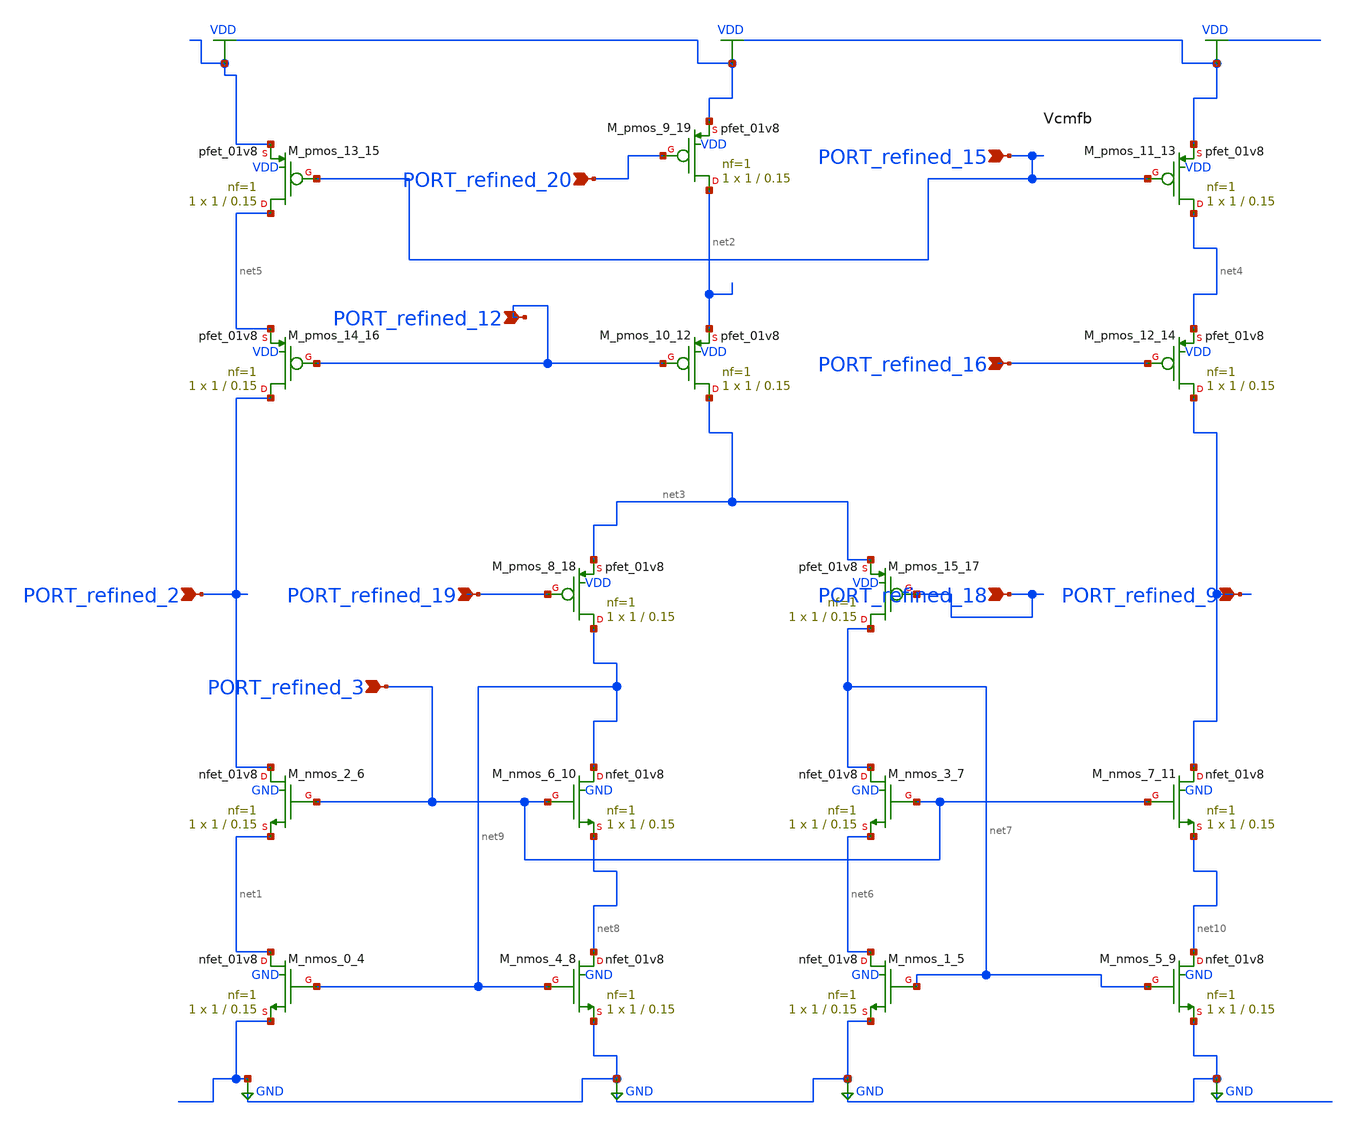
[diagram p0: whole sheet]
** sch_path: schematics/10_1587_elex_17_20200238_02_001_crop2.sch
**.subckt 10_1587_elex_17_20200238_02_001_crop2 PORT_refined_2 PORT_refined_18 PORT_refined_9
*+ PORT_refined_19 PORT_refined_20 PORT_refined_3 PORT_refined_12 PORT_refined_16 PORT_refined_15
*.ipin PORT_refined_2
*.ipin PORT_refined_18
*.ipin PORT_refined_9
*.ipin PORT_refined_19
*.ipin PORT_refined_20
*.ipin PORT_refined_3
*.ipin PORT_refined_12
*.ipin PORT_refined_16
*.ipin PORT_refined_15
XM_nmos_0_4 net1 net9 GND GND sky130_fd_pr__nfet_01v8 L=0.15 W=1 nf=1 ad='int((1 + 1)/2) * 1 / 1 * 0.29'
+ as='int((1 + 2)/2) * 1 / 1 * 0.29' pd='2*int((1 + 1)/2) * (1 / 1 + 0.29)' ps='2*int((1 + 2)/2) * (1 / 1 + 0.29)'
+ nrd='0.29 / 1 ' nrs='0.29 / 1 ' sa=0 sb=0 sd=0 mult=1 m=1
XM_nmos_1_5 net6 net7 GND GND sky130_fd_pr__nfet_01v8 L=0.15 W=1 nf=1 ad='int((1 + 1)/2) * 1 / 1 * 0.29'
+ as='int((1 + 2)/2) * 1 / 1 * 0.29' pd='2*int((1 + 1)/2) * (1 / 1 + 0.29)' ps='2*int((1 + 2)/2) * (1 / 1 + 0.29)'
+ nrd='0.29 / 1 ' nrs='0.29 / 1 ' sa=0 sb=0 sd=0 mult=1 m=1
XM_nmos_2_6 PORT_refined_2 PORT_refined_3 net1 GND sky130_fd_pr__nfet_01v8 L=0.15 W=1 nf=1 ad='int((1 + 1)/2) * 1 / 1 * 0.29'
+ as='int((1 + 2)/2) * 1 / 1 * 0.29' pd='2*int((1 + 1)/2) * (1 / 1 + 0.29)' ps='2*int((1 + 2)/2) * (1 / 1 + 0.29)'
+ nrd='0.29 / 1 ' nrs='0.29 / 1 ' sa=0 sb=0 sd=0 mult=1 m=1
XM_nmos_3_7 net7 PORT_refined_3 net6 GND sky130_fd_pr__nfet_01v8 L=0.15 W=1 nf=1 ad='int((1 + 1)/2) * 1 / 1 * 0.29'
+ as='int((1 + 2)/2) * 1 / 1 * 0.29' pd='2*int((1 + 1)/2) * (1 / 1 + 0.29)' ps='2*int((1 + 2)/2) * (1 / 1 + 0.29)'
+ nrd='0.29 / 1 ' nrs='0.29 / 1 ' sa=0 sb=0 sd=0 mult=1 m=1
XM_nmos_4_8 net8 net9 GND GND sky130_fd_pr__nfet_01v8 L=0.15 W=1 nf=1 ad='int((1 + 1)/2) * 1 / 1 * 0.29'
+ as='int((1 + 2)/2) * 1 / 1 * 0.29' pd='2*int((1 + 1)/2) * (1 / 1 + 0.29)' ps='2*int((1 + 2)/2) * (1 / 1 + 0.29)'
+ nrd='0.29 / 1 ' nrs='0.29 / 1 ' sa=0 sb=0 sd=0 mult=1 m=1
XM_nmos_5_9 net10 net7 GND GND sky130_fd_pr__nfet_01v8 L=0.15 W=1 nf=1 ad='int((1 + 1)/2) * 1 / 1 * 0.29'
+ as='int((1 + 2)/2) * 1 / 1 * 0.29' pd='2*int((1 + 1)/2) * (1 / 1 + 0.29)' ps='2*int((1 + 2)/2) * (1 / 1 + 0.29)'
+ nrd='0.29 / 1 ' nrs='0.29 / 1 ' sa=0 sb=0 sd=0 mult=1 m=1
XM_nmos_6_10 net9 PORT_refined_3 net8 GND sky130_fd_pr__nfet_01v8 L=0.15 W=1 nf=1 ad='int((1 + 1)/2) * 1 / 1 * 0.29'
+ as='int((1 + 2)/2) * 1 / 1 * 0.29' pd='2*int((1 + 1)/2) * (1 / 1 + 0.29)' ps='2*int((1 + 2)/2) * (1 / 1 + 0.29)'
+ nrd='0.29 / 1 ' nrs='0.29 / 1 ' sa=0 sb=0 sd=0 mult=1 m=1
XM_nmos_7_11 PORT_refined_9 PORT_refined_3 net10 GND sky130_fd_pr__nfet_01v8 L=0.15 W=1 nf=1 ad='int((1 + 1)/2) * 1 / 1 * 0.29'
+ as='int((1 + 2)/2) * 1 / 1 * 0.29' pd='2*int((1 + 1)/2) * (1 / 1 + 0.29)' ps='2*int((1 + 2)/2) * (1 / 1 + 0.29)'
+ nrd='0.29 / 1 ' nrs='0.29 / 1 ' sa=0 sb=0 sd=0 mult=1 m=1
XM_pmos_10_12 net3 PORT_refined_12 net2 VDD sky130_fd_pr__pfet_01v8 L=0.15 W=1 nf=1 ad='int((1 + 1)/2) * 1 / 1 * 0.29'
+ as='int((1 + 2)/2) * 1 / 1 * 0.29' pd='2*int((1 + 1)/2) * (1 / 1 + 0.29)' ps='2*int((1 + 2)/2) * (1 / 1 + 0.29)'
+ nrd='0.29 / 1 ' nrs='0.29 / 1 ' sa=0 sb=0 sd=0 mult=1 m=1
XM_pmos_11_13 net4 PORT_refined_15 VDD VDD sky130_fd_pr__pfet_01v8 L=0.15 W=1 nf=1 ad='int((1 + 1)/2) * 1 / 1 * 0.29'
+ as='int((1 + 2)/2) * 1 / 1 * 0.29' pd='2*int((1 + 1)/2) * (1 / 1 + 0.29)' ps='2*int((1 + 2)/2) * (1 / 1 + 0.29)'
+ nrd='0.29 / 1 ' nrs='0.29 / 1 ' sa=0 sb=0 sd=0 mult=1 m=1
XM_pmos_12_14 PORT_refined_9 PORT_refined_16 net4 VDD sky130_fd_pr__pfet_01v8 L=0.15 W=1 nf=1 ad='int((1 + 1)/2) * 1 / 1 * 0.29'
+ as='int((1 + 2)/2) * 1 / 1 * 0.29' pd='2*int((1 + 1)/2) * (1 / 1 + 0.29)' ps='2*int((1 + 2)/2) * (1 / 1 + 0.29)'
+ nrd='0.29 / 1 ' nrs='0.29 / 1 ' sa=0 sb=0 sd=0 mult=1 m=1
XM_pmos_13_15 net5 PORT_refined_15 VDD VDD sky130_fd_pr__pfet_01v8 L=0.15 W=1 nf=1 ad='int((1 + 1)/2) * 1 / 1 * 0.29'
+ as='int((1 + 2)/2) * 1 / 1 * 0.29' pd='2*int((1 + 1)/2) * (1 / 1 + 0.29)' ps='2*int((1 + 2)/2) * (1 / 1 + 0.29)'
+ nrd='0.29 / 1 ' nrs='0.29 / 1 ' sa=0 sb=0 sd=0 mult=1 m=1
XM_pmos_14_16 PORT_refined_2 PORT_refined_12 net5 VDD sky130_fd_pr__pfet_01v8 L=0.15 W=1 nf=1 ad='int((1 + 1)/2) * 1 / 1 * 0.29'
+ as='int((1 + 2)/2) * 1 / 1 * 0.29' pd='2*int((1 + 1)/2) * (1 / 1 + 0.29)' ps='2*int((1 + 2)/2) * (1 / 1 + 0.29)'
+ nrd='0.29 / 1 ' nrs='0.29 / 1 ' sa=0 sb=0 sd=0 mult=1 m=1
XM_pmos_15_17 net7 PORT_refined_18 net3 VDD sky130_fd_pr__pfet_01v8 L=0.15 W=1 nf=1 ad='int((1 + 1)/2) * 1 / 1 * 0.29'
+ as='int((1 + 2)/2) * 1 / 1 * 0.29' pd='2*int((1 + 1)/2) * (1 / 1 + 0.29)' ps='2*int((1 + 2)/2) * (1 / 1 + 0.29)'
+ nrd='0.29 / 1 ' nrs='0.29 / 1 ' sa=0 sb=0 sd=0 mult=1 m=1
XM_pmos_8_18 net9 PORT_refined_19 net3 VDD sky130_fd_pr__pfet_01v8 L=0.15 W=1 nf=1 ad='int((1 + 1)/2) * 1 / 1 * 0.29'
+ as='int((1 + 2)/2) * 1 / 1 * 0.29' pd='2*int((1 + 1)/2) * (1 / 1 + 0.29)' ps='2*int((1 + 2)/2) * (1 / 1 + 0.29)'
+ nrd='0.29 / 1 ' nrs='0.29 / 1 ' sa=0 sb=0 sd=0 mult=1 m=1
XM_pmos_9_19 net2 PORT_refined_20 VDD VDD sky130_fd_pr__pfet_01v8 L=0.15 W=1 nf=1 ad='int((1 + 1)/2) * 1 / 1 * 0.29'
+ as='int((1 + 2)/2) * 1 / 1 * 0.29' pd='2*int((1 + 1)/2) * (1 / 1 + 0.29)' ps='2*int((1 + 2)/2) * (1 / 1 + 0.29)'
+ nrd='0.29 / 1 ' nrs='0.29 / 1 ' sa=0 sb=0 sd=0 mult=1 m=1
**.ends
.GLOBAL GND
.GLOBAL VDD
.end
